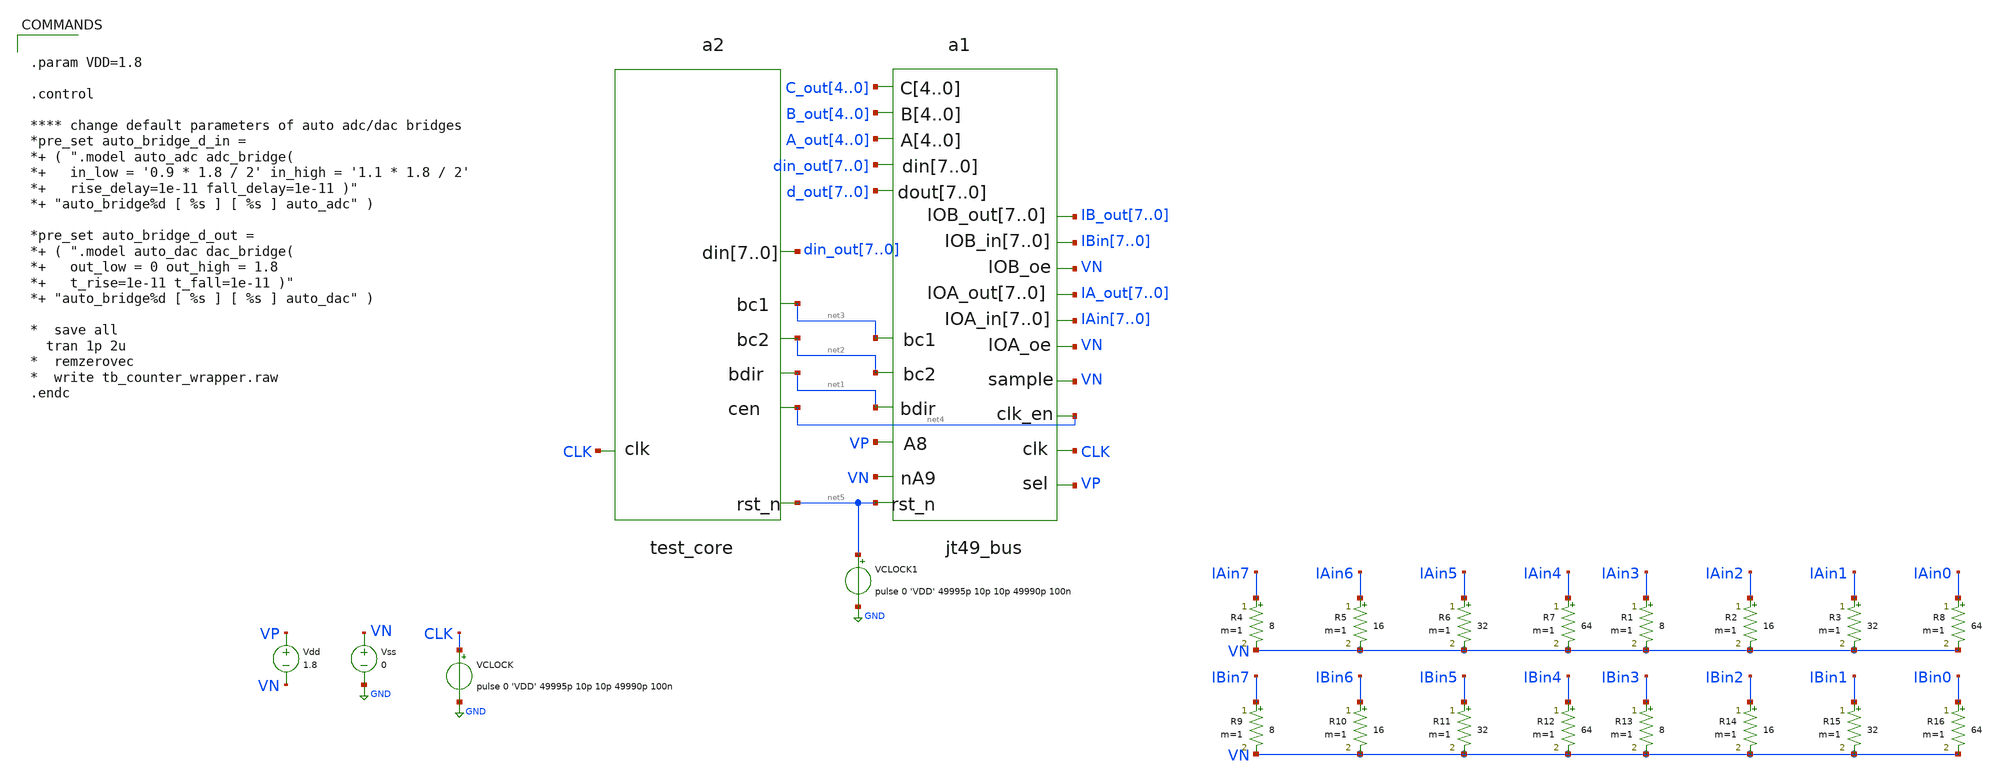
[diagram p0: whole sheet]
** sch_path: xschem/testbench.sch
**.subckt testbench
a1 [ net5 CLK net4 net1 net3 net2 din_out7 din_out6 din_out5 din_out4 din_out3 din_out2 din_out1
+ din_out0 VP IAin7 IAin6 IAin5 IAin4 IAin3 IAin2 IAin1 IAin0 IBin7 IBin6 IBin5 IBin4 IBin3 IBin2 IBin1 IBin0
+ VN VP ] [ d_out7 d_out6 d_out5 d_out4 d_out3 d_out2 d_out1 d_out0 A_out4 A_out3 A_out2 A_out1 A_out0
+ B_out4 B_out3 B_out2 B_out1 B_out0 C_out4 C_out3 C_out2 C_out1 C_out0 VN IA_out7 IA_out6 IA_out5 IA_out4
+ IA_out3 IA_out2 IA_out1 IA_out0 VN IB_out7 IB_out6 IB_out5 IB_out4 IB_out3 IB_out2 IB_out1 IB_out0 VN ]
+ jt49_bus
a2 [ CLK net5 ] [ net4 net1 net3 net2 din_out7 din_out6 din_out5 din_out4 din_out3 din_out2 din_out1
+ din_out0 ] test_core
VCLOCK CLK GND pulse 0 'VDD' 49995p 10p 10p 49990p 100n
Vdd VP VN 1.8
Vss VN GND 0
VCLOCK1 net5 GND pulse 0 'VDD' 49995p 10p 10p 49990p 100n
R4 IAin7 VN 8 m=1
R5 IAin6 VN 16 m=1
R6 IAin5 VN 32 m=1
R7 IAin4 VN 64 m=1
R1 IAin3 VN 8 m=1
R2 IAin2 VN 16 m=1
R3 IAin1 VN 32 m=1
R8 IAin0 VN 64 m=1
R9 IBin7 VN 8 m=1
R10 IBin6 VN 16 m=1
R11 IBin5 VN 32 m=1
R12 IBin4 VN 64 m=1
R13 IBin3 VN 8 m=1
R14 IBin2 VN 16 m=1
R15 IBin1 VN 32 m=1
R16 IBin0 VN 64 m=1
**** begin user architecture code


.param VDD=1.8

.control

**** change default parameters of auto adc/dac bridges
*pre_set auto_bridge_d_in =
*+ ( ".model auto_adc adc_bridge(
*+   in_low = '0.9 * 1.8 / 2' in_high = '1.1 * 1.8 / 2'
*+   rise_delay=1e-11 fall_delay=1e-11 )"
*+ "auto_bridge%d [ %s ] [ %s ] auto_adc" )

*pre_set auto_bridge_d_out =
*+ ( ".model auto_dac dac_bridge(
*+   out_low = 0 out_high = 1.8
*+   t_rise=1e-11 t_fall=1e-11 )"
*+ "auto_bridge%d [ %s ] [ %s ] auto_dac" )

*  save all
  tran 1p 2u
*  remzerovec
*  write tb_counter_wrapper.raw
.endc


**** end user architecture code
**.ends
.GLOBAL GND
**** begin user architecture code
.model test_core d_cosim simulation="ivlng" sim_args=["test_core"] delay=1e-12
.model jt49_bus d_cosim simulation="ivlng" sim_args=["jt49_bus"] delay=1e-12
**** end user architecture code
.end
